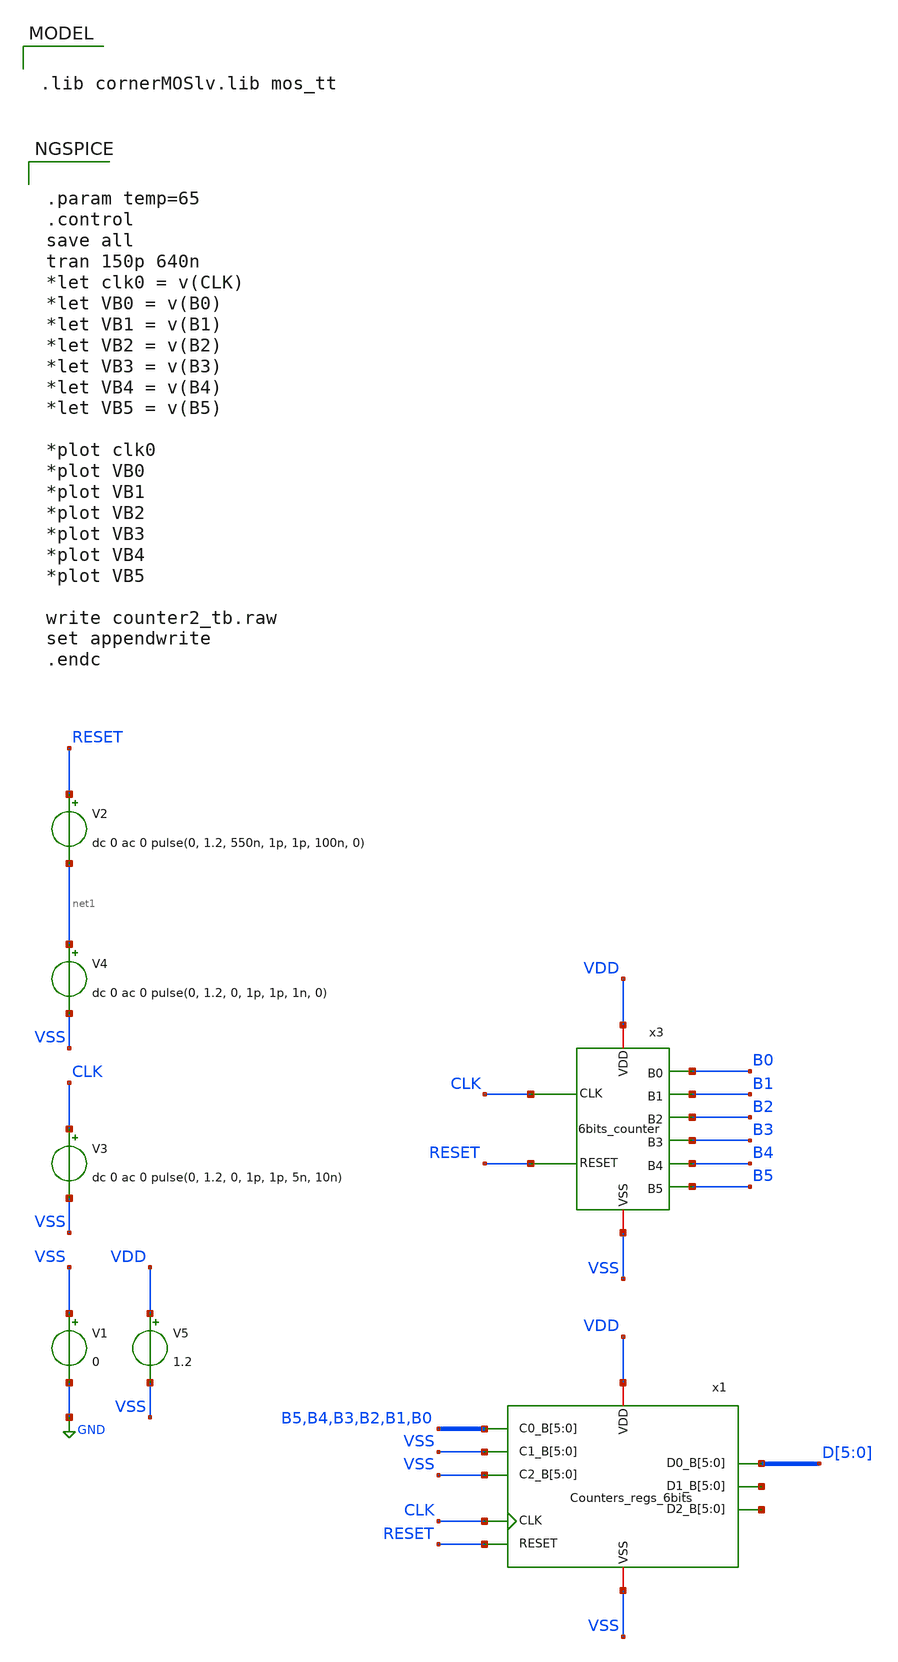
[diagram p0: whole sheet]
** sch_path: ADC8711-main/testbenches/tran/xschem/counter2_tb.sch
**.subckt counter2_tb
V1 VSS GND 0
V3 CLK VSS dc 0 ac 0 pulse(0, 1.2, 0, 1p, 1p, 5n, 10n)
V5 VDD VSS 1.2
V4 net1 VSS dc 0 ac 0 pulse(0, 1.2, 0, 1p, 1p, 1n, 0)
x3 B0 CLK VDD B1 B2 VSS RESET B3 B4 B5 6bits_counter
x1 RESET D[5] D[4] D[3] D[2] D[1] D[0] VDD CLK VSS net2[5] net2[4] net2[3] net2[2] net2[1] net2[0]
+ net3[5] net3[4] net3[3] net3[2] net3[1] net3[0] B5 B4 B3 B2 B1 B0 VSS VSS VSS VSS VSS VSS VSS VSS VSS VSS
+ VSS VSS Counters_regs_6bits
V2 RESET net1 dc 0 ac 0 pulse(0, 1.2, 550n, 1p, 1p, 100n, 0)
**** begin user architecture code


.param temp=65
.control
save all
tran 150p 640n
*let clk0 = v(CLK)
*let VB0 = v(B0)
*let VB1 = v(B1)
*let VB2 = v(B2)
*let VB3 = v(B3)
*let VB4 = v(B4)
*let VB5 = v(B5)

*plot clk0
*plot VB0
*plot VB1
*plot VB2
*plot VB3
*plot VB4
*plot VB5

write counter2_tb.raw
set appendwrite
.endc



.lib cornerMOSlv.lib mos_tt

**** end user architecture code
**.ends
.GLOBAL GND
.end
